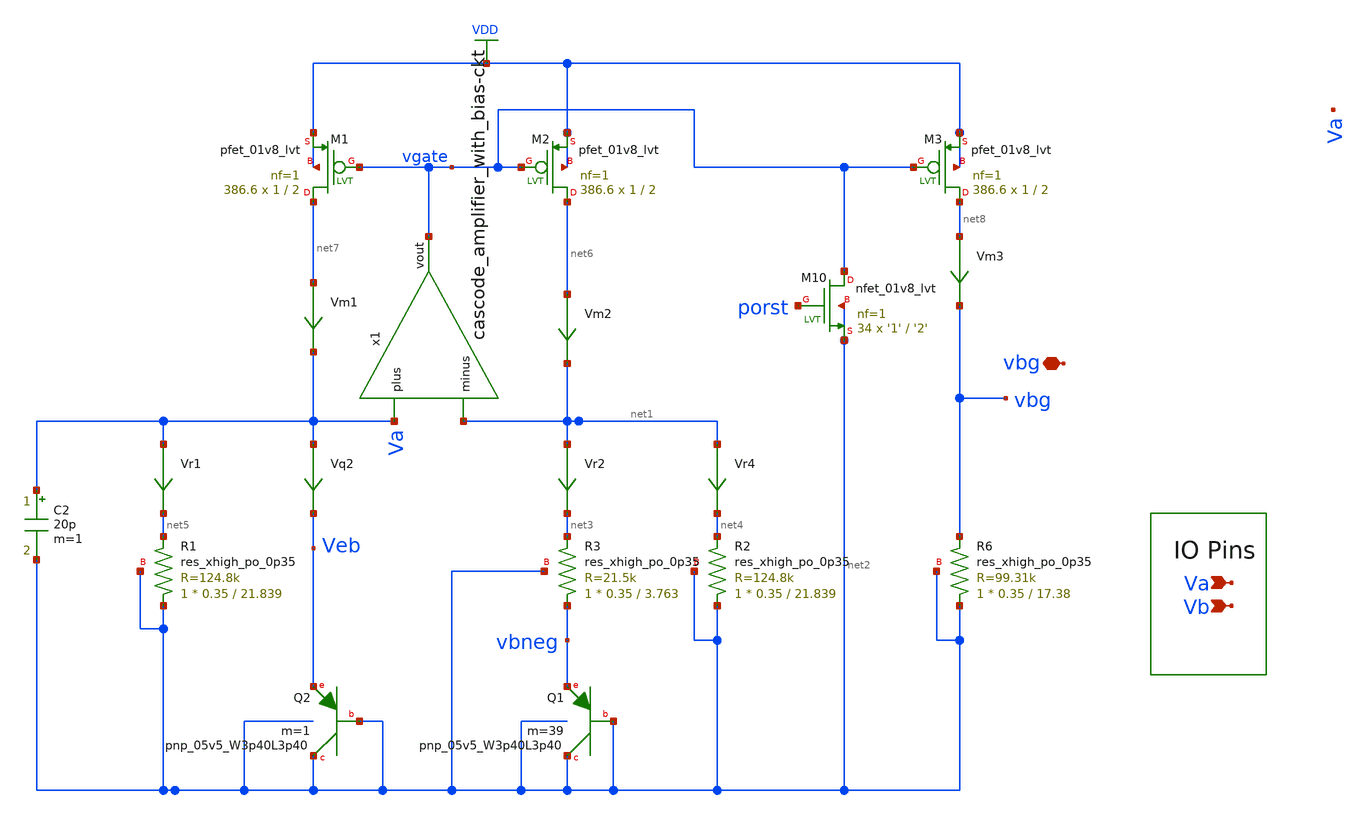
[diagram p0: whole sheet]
** sch_path: bandgap_sky130_v1/cascode_bandgapCore.sch
**.subckt cascode_bandgapCore Va Vb vbg
*.ipin Va
*.ipin Vb
*.iopin vbg
XQ2 net2 net2 Veb sky130_fd_pr__pnp_05v5_W3p40L3p40 m=1
Vr4 net1 net4 0
.save i(vr4)
Vr2 net1 net3 0
.save i(vr2)
Vr1 Va net5 0
.save i(vr1)
Vq2 Va Veb 0
.save i(vq2)
XQ1 net2 net2 vbneg sky130_fd_pr__pnp_05v5_W3p40L3p40 m=39
XR1 net2 net5 net2 sky130_fd_pr__res_xhigh_po_0p35 L=21.839 mult=1 m=1
XR2 net2 net4 net2 sky130_fd_pr__res_xhigh_po_0p35 L=21.839 mult=1 m=1
XR3 vbneg net3 net2 sky130_fd_pr__res_xhigh_po_0p35 L=3.763 mult=1 m=1
XR6 net2 vbg net2 sky130_fd_pr__res_xhigh_po_0p35 L=17.38 mult=1 m=1
x1 Va net1 vgate cascode_amplifier_with_bias-ckt
C2 Va net2 20p m=1
Vm1 net7 Va 0
.save i(vm1)
Vm2 net6 net1 0
.save i(vm2)
XM1 net7 vgate VDD VDD sky130_fd_pr__pfet_01v8_lvt L=2 W=1 nf=1 ad='int((nf+1)/2) * W/nf * 0.29' as='int((nf+2)/2) * W/nf * 0.29'
+ pd='2*int((nf+1)/2) * (W/nf + 0.29)' ps='2*int((nf+2)/2) * (W/nf + 0.29)' nrd='0.29 / W' nrs='0.29 / W'
+ sa=0 sb=0 sd=0 mult=386.6 m=386.6
XM2 net6 vgate VDD VDD sky130_fd_pr__pfet_01v8_lvt L=2 W=1 nf=1 ad='int((nf+1)/2) * W/nf * 0.29' as='int((nf+2)/2) * W/nf * 0.29'
+ pd='2*int((nf+1)/2) * (W/nf + 0.29)' ps='2*int((nf+2)/2) * (W/nf + 0.29)' nrd='0.29 / W' nrs='0.29 / W'
+ sa=0 sb=0 sd=0 mult=386.6 m=386.6
XM10 vgate porst net2 net2 sky130_fd_pr__nfet_01v8_lvt L='2' W='1' nf=1 ad='int((nf+1)/2) * W/nf * 0.29'
+ as='int((nf+2)/2) * W/nf * 0.29' pd='2*int((nf+1)/2) * (W/nf + 0.29)' ps='2*int((nf+2)/2) * (W/nf + 0.29)'
+ nrd='0.29 / W' nrs='0.29 / W' sa=0 sb=0 sd=0 mult=34 m=34
Vm3 net8 vbg 0
.save i(vm3)
XM3 net8 vgate VDD VDD sky130_fd_pr__pfet_01v8_lvt L=2 W=1 nf=1 ad='int((nf+1)/2) * W/nf * 0.29' as='int((nf+2)/2) * W/nf * 0.29'
+ pd='2*int((nf+1)/2) * (W/nf + 0.29)' ps='2*int((nf+2)/2) * (W/nf + 0.29)' nrd='0.29 / W' nrs='0.29 / W'
+ sa=0 sb=0 sd=0 mult=386.6 m=386.6
**.ends

* expanding   symbol:  bandgap_sky130_v1/cascode_amplifier_with_bias-ckt.sym # of pins=3
** sym_path: bandgap_sky130_v1/cascode_amplifier_with_bias-ckt.sym
** sch_path: bandgap_sky130_v1/cascode_amplifier_with_bias-ckt.sch
.subckt cascode_amplifier_with_bias-ckt plus minus vout
*.ipin plus
*.ipin minus
*.opin vout
XM5 vout plus Vq GND sky130_fd_pr__nfet_01v8_lvt L='2' W='1' nf=1 ad='int((nf+1)/2) * W/nf * 0.29' as='int((nf+2)/2) * W/nf * 0.29'
+ pd='2*int((nf+1)/2) * (W/nf + 0.29)' ps='2*int((nf+2)/2) * (W/nf + 0.29)' nrd='0.29 / W' nrs='0.29 / W'
+ sa=0 sb=0 sd=0 mult=26.95 m=26.95
XM6 Vq Vx GND GND sky130_fd_pr__nfet_01v8_lvt L=2 W=1 nf=1 ad='int((nf+1)/2) * W/nf * 0.29' as='int((nf+2)/2) * W/nf * 0.29'
+ pd='2*int((nf+1)/2) * (W/nf + 0.29)' ps='2*int((nf+2)/2) * (W/nf + 0.29)' nrd='0.29 / W' nrs='0.29 / W'
+ sa=0 sb=0 sd=0 mult=3.65 m=3.65
XM9 vg minus Vq GND sky130_fd_pr__nfet_01v8_lvt L='2' W='1' nf=1 ad='int((nf+1)/2) * W/nf * 0.29' as='int((nf+2)/2) * W/nf * 0.29'
+ pd='2*int((nf+1)/2) * (W/nf + 0.29)' ps='2*int((nf+2)/2) * (W/nf + 0.29)' nrd='0.29 / W' nrs='0.29 / W'
+ sa=0 sb=0 sd=0 mult=26.95 m=26.95
XM7 Vx Vx GND GND sky130_fd_pr__nfet_01v8_lvt L=2 W=1 nf=1 ad='int((nf+1)/2) * W/nf * 0.29' as='int((nf+2)/2) * W/nf * 0.29'
+ pd='2*int((nf+1)/2) * (W/nf + 0.29)' ps='2*int((nf+2)/2) * (W/nf + 0.29)' nrd='0.29 / W' nrs='0.29 / W'
+ sa=0 sb=0 sd=0 mult=3.65 m=3.65
XM13 Vx vout VDD VDD sky130_fd_pr__pfet_01v8_lvt L=2 W=1 nf=1 ad='int((nf+1)/2) * W/nf * 0.29' as='int((nf+2)/2) * W/nf * 0.29'
+ pd='2*int((nf+1)/2) * (W/nf + 0.29)' ps='2*int((nf+2)/2) * (W/nf + 0.29)' nrd='0.29 / W' nrs='0.29 / W'
+ sa=0 sb=0 sd=0 mult=77.32 m=77.32
XM4 vg vg VDD VDD sky130_fd_pr__pfet_01v8_lvt L=2 W=1 nf=1 ad='int((nf+1)/2) * W/nf * 0.29' as='int((nf+2)/2) * W/nf * 0.29'
+ pd='2*int((nf+1)/2) * (W/nf + 0.29)' ps='2*int((nf+2)/2) * (W/nf + 0.29)' nrd='0.29 / W' nrs='0.29 / W'
+ sa=0 sb=0 sd=0 mult=38.66 m=38.66
XM8 vout vg VDD VDD sky130_fd_pr__pfet_01v8_lvt L=2 W=1 nf=1 ad='int((nf+1)/2) * W/nf * 0.29' as='int((nf+2)/2) * W/nf * 0.29'
+ pd='2*int((nf+1)/2) * (W/nf + 0.29)' ps='2*int((nf+2)/2) * (W/nf + 0.29)' nrd='0.29 / W' nrs='0.29 / W'
+ sa=0 sb=0 sd=0 mult=38.66 m=38.66
.ends

.GLOBAL VDD
.GLOBAL GND
.end
